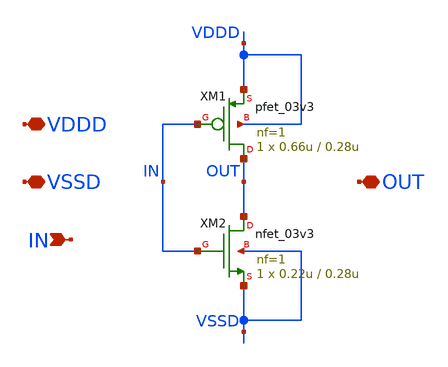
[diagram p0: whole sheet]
** sch_path: SAR_ADC/blocks/SAR_clock/clock_generator_inv_1x.sch
**.subckt clock_generator_inv_1x VDDD VSSD OUT IN
*.iopin VDDD
*.iopin VSSD
*.iopin OUT
*.ipin IN
XM1 OUT IN VDDD VDDD pfet_03v3 L=0.28u W=0.66u nf=1 ad='int((nf+1)/2) * W/nf * 0.18u' as='int((nf+2)/2) * W/nf * 0.18u'
+ pd='2*int((nf+1)/2) * (W/nf + 0.18u)' ps='2*int((nf+2)/2) * (W/nf + 0.18u)' nrd='0.18u / W' nrs='0.18u / W'
+ sa=0 sb=0 sd=0 m=1
XM2 OUT IN VSSD VSSD nfet_03v3 L=0.28u W=0.22u nf=1 ad='int((nf+1)/2) * W/nf * 0.18u' as='int((nf+2)/2) * W/nf * 0.18u'
+ pd='2*int((nf+1)/2) * (W/nf + 0.18u)' ps='2*int((nf+2)/2) * (W/nf + 0.18u)' nrd='0.18u / W' nrs='0.18u / W'
+ sa=0 sb=0 sd=0 m=1
**.ends
.end
